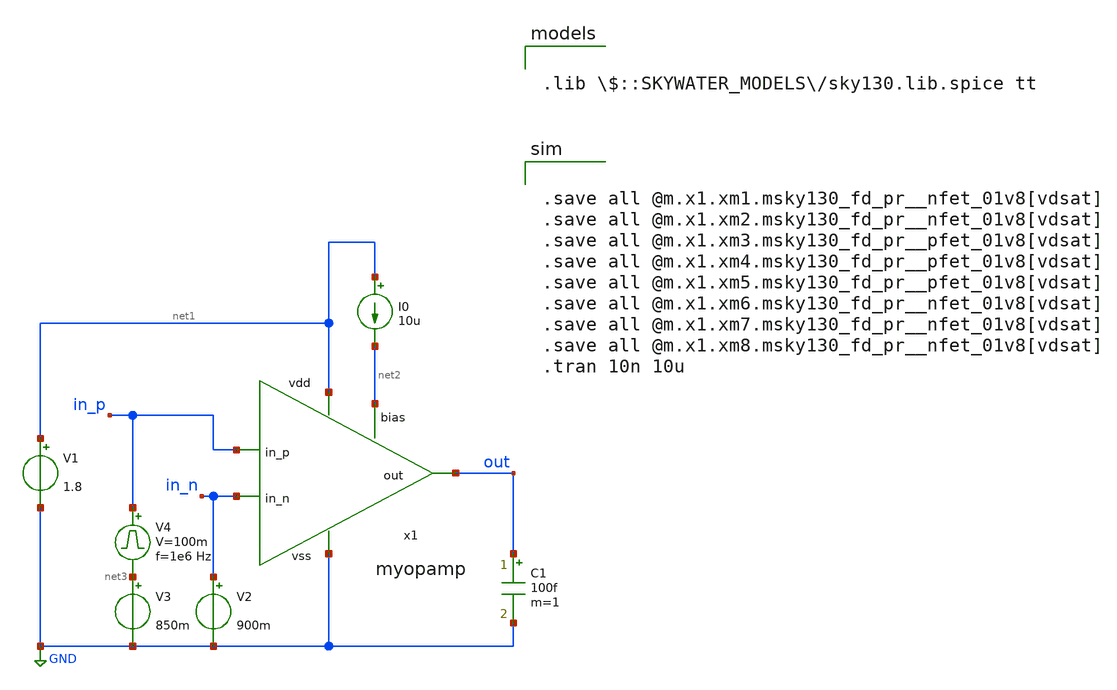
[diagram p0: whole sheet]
** sch_path: design/myopamp/test/tb.sch
**.subckt tb
x1 net1 in_n in_p out net2 GND myopamp
V1 net1 GND 1.8
I0 net1 net2 10u
V2 in_n GND 900m
V3 net3 GND 850m
V4 in_p net3 pulse 0 100m '0.495/ 1e6 ' '0.01/1e6 ' '0.01/1e6 ' '0.49/1e6 ' '1/1e6 '
C1 out GND 100f m=1
**** begin user architecture code


.save all @m.x1.xm1.msky130_fd_pr__nfet_01v8[vdsat]
.save all @m.x1.xm2.msky130_fd_pr__nfet_01v8[vdsat]
.save all @m.x1.xm3.msky130_fd_pr__pfet_01v8[vdsat]
.save all @m.x1.xm4.msky130_fd_pr__pfet_01v8[vdsat]
.save all @m.x1.xm5.msky130_fd_pr__pfet_01v8[vdsat]
.save all @m.x1.xm6.msky130_fd_pr__nfet_01v8[vdsat]
.save all @m.x1.xm7.msky130_fd_pr__nfet_01v8[vdsat]
.save all @m.x1.xm8.msky130_fd_pr__nfet_01v8[vdsat]
.tran 10n 10u



.lib $::SKYWATER_MODELS/sky130.lib.spice tt

**** end user architecture code
**.ends

* expanding   symbol:  myopamp/myopamp.sym # of pins=6
** sym_path: design/myopamp/myopamp.sym
** sch_path: design/myopamp/myopamp.sch
.subckt myopamp vdd in_n in_p out bias vss
*.ipin in_n
*.ipin in_p
*.ipin bias
*.opin out
*.iopin vdd
*.iopin vss
XM7 vdd net2 net3 vdd sky130_fd_pr__pfet_g5v0d10v5 L=2 W=2 nf=1 ad='int((nf+1)/2) * W/nf * 0.29' as='int((nf+2)/2) * W/nf * 0.29'
+ pd='2*int((nf+1)/2) * (W/nf + 0.29)' ps='2*int((nf+2)/2) * (W/nf + 0.29)' nrd='0.29 / W' nrs='0.29 / W'
+ sa=0 sb=0 sd=0 mult=2 m=2
XM6 vdd net2 net2 vdd sky130_fd_pr__pfet_g5v0d10v5 L=2 W=2 nf=1 ad='int((nf+1)/2) * W/nf * 0.29' as='int((nf+2)/2) * W/nf * 0.29'
+ pd='2*int((nf+1)/2) * (W/nf + 0.29)' ps='2*int((nf+2)/2) * (W/nf + 0.29)' nrd='0.29 / W' nrs='0.29 / W'
+ sa=0 sb=0 sd=0 mult=2 m=2
XM8 vdd net3 out vdd sky130_fd_pr__pfet_g5v0d10v5 L=2 W=2 nf=1 ad='int((nf+1)/2) * W/nf * 0.29' as='int((nf+2)/2) * W/nf * 0.29'
+ pd='2*int((nf+1)/2) * (W/nf + 0.29)' ps='2*int((nf+2)/2) * (W/nf + 0.29)' nrd='0.29 / W' nrs='0.29 / W'
+ sa=0 sb=0 sd=0 mult=16 m=16
XM4 net2 in_n net1 vss sky130_fd_pr__nfet_g5v0d10v5 L=1 W=10 nf=1 ad='int((nf+1)/2) * W/nf * 0.29' as='int((nf+2)/2) * W/nf * 0.29'
+ pd='2*int((nf+1)/2) * (W/nf + 0.29)' ps='2*int((nf+2)/2) * (W/nf + 0.29)' nrd='0.29 / W' nrs='0.29 / W'
+ sa=0 sb=0 sd=0 mult=4 m=4
XM5 net3 in_p net1 vss sky130_fd_pr__nfet_g5v0d10v5 L=1 W=10 nf=1 ad='int((nf+1)/2) * W/nf * 0.29' as='int((nf+2)/2) * W/nf * 0.29'
+ pd='2*int((nf+1)/2) * (W/nf + 0.29)' ps='2*int((nf+2)/2) * (W/nf + 0.29)' nrd='0.29 / W' nrs='0.29 / W'
+ sa=0 sb=0 sd=0 mult=10 m=10
XM1 bias bias vss vss sky130_fd_pr__nfet_g5v0d10v5 L=2 W=1 nf=1 ad='int((nf+1)/2) * W/nf * 0.29' as='int((nf+2)/2) * W/nf * 0.29'
+ pd='2*int((nf+1)/2) * (W/nf + 0.29)' ps='2*int((nf+2)/2) * (W/nf + 0.29)' nrd='0.29 / W' nrs='0.29 / W'
+ sa=0 sb=0 sd=0 mult=2 m=2
XM2 net1 bias vss vss sky130_fd_pr__nfet_g5v0d10v5 L=2 W=1 nf=1 ad='int((nf+1)/2) * W/nf * 0.29' as='int((nf+2)/2) * W/nf * 0.29'
+ pd='2*int((nf+1)/2) * (W/nf + 0.29)' ps='2*int((nf+2)/2) * (W/nf + 0.29)' nrd='0.29 / W' nrs='0.29 / W'
+ sa=0 sb=0 sd=0 mult=2 m=2
XM3 out bias vss vss sky130_fd_pr__nfet_g5v0d10v5 L=2 W=1 nf=1 ad='int((nf+1)/2) * W/nf * 0.29' as='int((nf+2)/2) * W/nf * 0.29'
+ pd='2*int((nf+1)/2) * (W/nf + 0.29)' ps='2*int((nf+2)/2) * (W/nf + 0.29)' nrd='0.29 / W' nrs='0.29 / W'
+ sa=0 sb=0 sd=0 mult=16 m=16
XC1 net3 net4 sky130_fd_pr__cap_mim_m3_1 W=10 L=10 MF=4 m=4
XR1 out net4 vss sky130_fd_pr__res_xhigh_po_0p69 L=1 mult=1 m=1
.ends

.GLOBAL GND
.end
